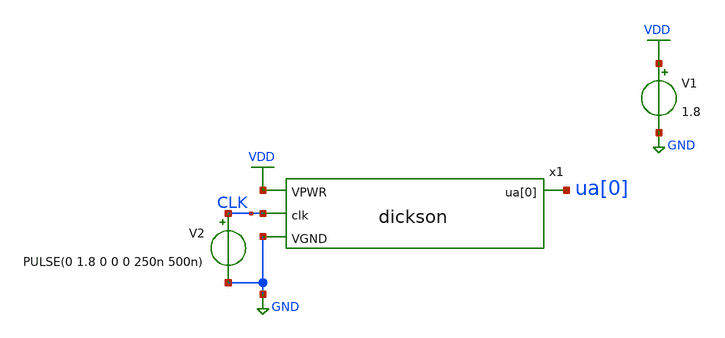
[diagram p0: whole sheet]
** sch_path: xschem/testbench.sch
**.subckt testbench
x1 VDD CLK ua[0] GND dickson
V1 VDD GND 1.8
V2 CLK GND PULSE(0 1.8 0 0 0 250n 500n)
**** begin user architecture code

** opencircuitdesign pdks install
.lib $::SKYWATER_MODELS/sky130.lib.spice tt





.tran 10n 100u
.save all

.control
run
write testbench.raw
.endc


**** end user architecture code
**.ends

* expanding   symbol:  dickson.sym # of pins=4
** sym_path: xschem/dickson.sym
** sch_path: xschem/dickson.sch
.subckt dickson VPWR clk ua[0] VGND
*.ipin clk
*.opin ua[0]
*.ipin VPWR
*.ipin VGND
XM1 clka clk VPWR VDD sky130_fd_pr__pfet_01v8 L=0.45 W=1.5 nf=1 ad='int((nf+1)/2) * W/nf * 0.29' as='int((nf+2)/2) * W/nf * 0.29'
+ pd='2*int((nf+1)/2) * (W/nf + 0.29)' ps='2*int((nf+2)/2) * (W/nf + 0.29)' nrd='0.29 / W' nrs='0.29 / W'
+ sa=0 sb=0 sd=0 mult=1 m=1
XM3 clka clk VGND GND sky130_fd_pr__nfet_01v8 L=0.45 W=1 nf=1 ad='int((nf+1)/2) * W/nf * 0.29' as='int((nf+2)/2) * W/nf * 0.29'
+ pd='2*int((nf+1)/2) * (W/nf + 0.29)' ps='2*int((nf+2)/2) * (W/nf + 0.29)' nrd='0.29 / W' nrs='0.29 / W'
+ sa=0 sb=0 sd=0 mult=1 m=1
XM2 clkb clka VPWR VDD sky130_fd_pr__pfet_01v8 L=0.45 W=1.5 nf=1 ad='int((nf+1)/2) * W/nf * 0.29' as='int((nf+2)/2) * W/nf * 0.29'
+ pd='2*int((nf+1)/2) * (W/nf + 0.29)' ps='2*int((nf+2)/2) * (W/nf + 0.29)' nrd='0.29 / W' nrs='0.29 / W'
+ sa=0 sb=0 sd=0 mult=1 m=1
XM4 clkb clka VGND GND sky130_fd_pr__nfet_01v8 L=0.45 W=1 nf=1 ad='int((nf+1)/2) * W/nf * 0.29' as='int((nf+2)/2) * W/nf * 0.29'
+ pd='2*int((nf+1)/2) * (W/nf + 0.29)' ps='2*int((nf+2)/2) * (W/nf + 0.29)' nrd='0.29 / W' nrs='0.29 / W'
+ sa=0 sb=0 sd=0 mult=1 m=1
XC3 clka stage3 sky130_fd_pr__cap_mim_m3_1 W=25 L=25 MF=1 m=1
XM5 stage1 VPWR VPWR VPWR sky130_fd_pr__nfet_01v8_lvt L=8 W=7 nf=1 ad='int((nf+1)/2) * W/nf * 0.29' as='int((nf+2)/2) * W/nf * 0.29'
+ pd='2*int((nf+1)/2) * (W/nf + 0.29)' ps='2*int((nf+2)/2) * (W/nf + 0.29)' nrd='0.29 / W' nrs='0.29 / W'
+ sa=0 sb=0 sd=0 mult=1 m=1
XC1 clka stage1 sky130_fd_pr__cap_mim_m3_1 W=25 L=25 MF=1 m=1
XM6 stage2 stage1 stage1 stage1 sky130_fd_pr__nfet_01v8_lvt L=8 W=7 nf=1 ad='int((nf+1)/2) * W/nf * 0.29'
+ as='int((nf+2)/2) * W/nf * 0.29' pd='2*int((nf+1)/2) * (W/nf + 0.29)' ps='2*int((nf+2)/2) * (W/nf + 0.29)'
+ nrd='0.29 / W' nrs='0.29 / W' sa=0 sb=0 sd=0 mult=1 m=1
XM7 stage3 stage2 stage2 stage2 sky130_fd_pr__nfet_01v8_lvt L=8 W=7 nf=1 ad='int((nf+1)/2) * W/nf * 0.29'
+ as='int((nf+2)/2) * W/nf * 0.29' pd='2*int((nf+1)/2) * (W/nf + 0.29)' ps='2*int((nf+2)/2) * (W/nf + 0.29)'
+ nrd='0.29 / W' nrs='0.29 / W' sa=0 sb=0 sd=0 mult=1 m=1
XC2 clkb stage2 sky130_fd_pr__cap_mim_m3_1 W=25 L=25 MF=1 m=1
XM8 vout stage3 stage3 stage3 sky130_fd_pr__nfet_01v8_lvt L=8 W=7 nf=1 ad='int((nf+1)/2) * W/nf * 0.29'
+ as='int((nf+2)/2) * W/nf * 0.29' pd='2*int((nf+1)/2) * (W/nf + 0.29)' ps='2*int((nf+2)/2) * (W/nf + 0.29)'
+ nrd='0.29 / W' nrs='0.29 / W' sa=0 sb=0 sd=0 mult=1 m=1
XC4 VGND vout sky130_fd_pr__cap_mim_m3_1 W=30 L=25 MF=1 m=1
XR2 ua[0] vout VGND sky130_fd_pr__res_xhigh_po_0p35 L=2500 mult=1 m=1
XR1 VGND ua[0] VGND sky130_fd_pr__res_xhigh_po_0p35 L=500 mult=1 m=1
.ends

.GLOBAL GND
.GLOBAL VDD
.end
